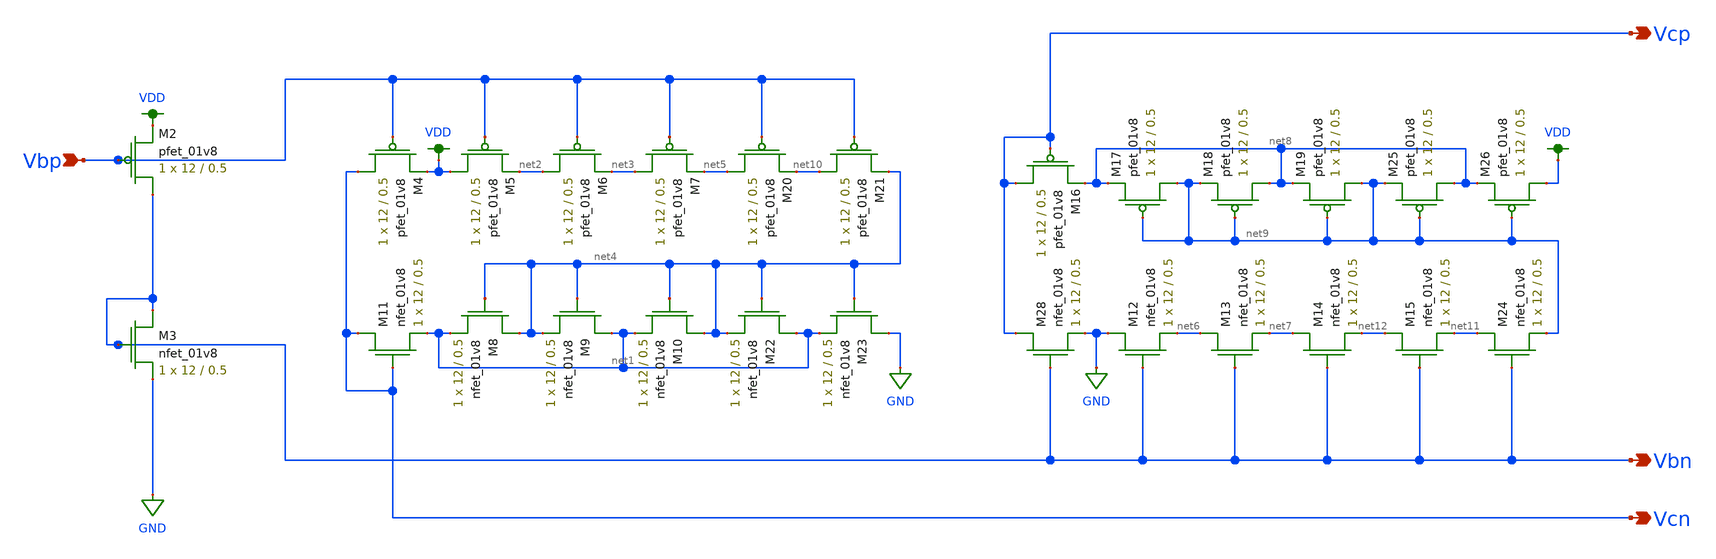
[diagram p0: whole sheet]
** sch_path: bias_current_generator.sch
**.subckt bias_current_generator Vcn Vbn Vcp Vbp
*.opin Vcn
*.opin Vbn
*.opin Vcp
*.ipin Vbp
XM4 Vcn Vbp VDD VDD sky130_fd_pr__pfet_01v8 L=0.5 W=12 nf=1 ad='int((nf+1)/2) * W/nf * 0.29' as='int((nf+2)/2) * W/nf * 0.29'
+ pd='2*int((nf+1)/2) * (W/nf + 0.29)' ps='2*int((nf+2)/2) * (W/nf + 0.29)' nrd='0.29 / W' nrs='0.29 / W'
+ sa=0 sb=0 sd=0 mult=1 m=1
XM11 Vcn Vcn net1 GND sky130_fd_pr__nfet_01v8 L=0.5 W=12 nf=1 ad='int((nf+1)/2) * W/nf * 0.29' as='int((nf+2)/2) * W/nf * 0.29'
+ pd='2*int((nf+1)/2) * (W/nf + 0.29)' ps='2*int((nf+2)/2) * (W/nf + 0.29)' nrd='0.29 / W' nrs='0.29 / W'
+ sa=0 sb=0 sd=0 mult=1 m=1
XM8 net4 net4 net1 GND sky130_fd_pr__nfet_01v8 L=0.5 W=12 nf=1 ad='int((nf+1)/2) * W/nf * 0.29' as='int((nf+2)/2) * W/nf * 0.29'
+ pd='2*int((nf+1)/2) * (W/nf + 0.29)' ps='2*int((nf+2)/2) * (W/nf + 0.29)' nrd='0.29 / W' nrs='0.29 / W'
+ sa=0 sb=0 sd=0 mult=1 m=1
XM9 net1 net4 net4 GND sky130_fd_pr__nfet_01v8 L=0.5 W=12 nf=1 ad='int((nf+1)/2) * W/nf * 0.29' as='int((nf+2)/2) * W/nf * 0.29'
+ pd='2*int((nf+1)/2) * (W/nf + 0.29)' ps='2*int((nf+2)/2) * (W/nf + 0.29)' nrd='0.29 / W' nrs='0.29 / W'
+ sa=0 sb=0 sd=0 mult=1 m=1
XM10 net4 net4 net1 GND sky130_fd_pr__nfet_01v8 L=0.5 W=12 nf=1 ad='int((nf+1)/2) * W/nf * 0.29' as='int((nf+2)/2) * W/nf * 0.29'
+ pd='2*int((nf+1)/2) * (W/nf + 0.29)' ps='2*int((nf+2)/2) * (W/nf + 0.29)' nrd='0.29 / W' nrs='0.29 / W'
+ sa=0 sb=0 sd=0 mult=1 m=1
XM22 net1 net4 net4 GND sky130_fd_pr__nfet_01v8 L=0.5 W=12 nf=1 ad='int((nf+1)/2) * W/nf * 0.29' as='int((nf+2)/2) * W/nf * 0.29'
+ pd='2*int((nf+1)/2) * (W/nf + 0.29)' ps='2*int((nf+2)/2) * (W/nf + 0.29)' nrd='0.29 / W' nrs='0.29 / W'
+ sa=0 sb=0 sd=0 mult=1 m=1
XM23 GND net4 net1 GND sky130_fd_pr__nfet_01v8 L=0.5 W=12 nf=1 ad='int((nf+1)/2) * W/nf * 0.29' as='int((nf+2)/2) * W/nf * 0.29'
+ pd='2*int((nf+1)/2) * (W/nf + 0.29)' ps='2*int((nf+2)/2) * (W/nf + 0.29)' nrd='0.29 / W' nrs='0.29 / W'
+ sa=0 sb=0 sd=0 mult=1 m=1
XM28 Vcp Vbn GND GND sky130_fd_pr__nfet_01v8 L=0.5 W=12 nf=1 ad='int((nf+1)/2) * W/nf * 0.29' as='int((nf+2)/2) * W/nf * 0.29'
+ pd='2*int((nf+1)/2) * (W/nf + 0.29)' ps='2*int((nf+2)/2) * (W/nf + 0.29)' nrd='0.29 / W' nrs='0.29 / W'
+ sa=0 sb=0 sd=0 mult=1 m=1
XM12 GND Vbn net6 GND sky130_fd_pr__nfet_01v8 L=0.5 W=12 nf=1 ad='int((nf+1)/2) * W/nf * 0.29' as='int((nf+2)/2) * W/nf * 0.29'
+ pd='2*int((nf+1)/2) * (W/nf + 0.29)' ps='2*int((nf+2)/2) * (W/nf + 0.29)' nrd='0.29 / W' nrs='0.29 / W'
+ sa=0 sb=0 sd=0 mult=1 m=1
XM13 net6 Vbn net7 GND sky130_fd_pr__nfet_01v8 L=0.5 W=12 nf=1 ad='int((nf+1)/2) * W/nf * 0.29' as='int((nf+2)/2) * W/nf * 0.29'
+ pd='2*int((nf+1)/2) * (W/nf + 0.29)' ps='2*int((nf+2)/2) * (W/nf + 0.29)' nrd='0.29 / W' nrs='0.29 / W'
+ sa=0 sb=0 sd=0 mult=1 m=1
XM14 net7 Vbn net12 GND sky130_fd_pr__nfet_01v8 L=0.5 W=12 nf=1 ad='int((nf+1)/2) * W/nf * 0.29' as='int((nf+2)/2) * W/nf * 0.29'
+ pd='2*int((nf+1)/2) * (W/nf + 0.29)' ps='2*int((nf+2)/2) * (W/nf + 0.29)' nrd='0.29 / W' nrs='0.29 / W'
+ sa=0 sb=0 sd=0 mult=1 m=1
XM15 net12 Vbn net11 GND sky130_fd_pr__nfet_01v8 L=0.5 W=12 nf=1 ad='int((nf+1)/2) * W/nf * 0.29' as='int((nf+2)/2) * W/nf * 0.29'
+ pd='2*int((nf+1)/2) * (W/nf + 0.29)' ps='2*int((nf+2)/2) * (W/nf + 0.29)' nrd='0.29 / W' nrs='0.29 / W'
+ sa=0 sb=0 sd=0 mult=1 m=1
XM24 net11 Vbn net9 GND sky130_fd_pr__nfet_01v8 L=0.5 W=12 nf=1 ad='int((nf+1)/2) * W/nf * 0.29' as='int((nf+2)/2) * W/nf * 0.29'
+ pd='2*int((nf+1)/2) * (W/nf + 0.29)' ps='2*int((nf+2)/2) * (W/nf + 0.29)' nrd='0.29 / W' nrs='0.29 / W'
+ sa=0 sb=0 sd=0 mult=1 m=1
XM5 VDD Vbp net2 VDD sky130_fd_pr__pfet_01v8 L=0.5 W=12 nf=1 ad='int((nf+1)/2) * W/nf * 0.29' as='int((nf+2)/2) * W/nf * 0.29'
+ pd='2*int((nf+1)/2) * (W/nf + 0.29)' ps='2*int((nf+2)/2) * (W/nf + 0.29)' nrd='0.29 / W' nrs='0.29 / W'
+ sa=0 sb=0 sd=0 mult=1 m=1
XM6 net2 Vbp net3 VDD sky130_fd_pr__pfet_01v8 L=0.5 W=12 nf=1 ad='int((nf+1)/2) * W/nf * 0.29' as='int((nf+2)/2) * W/nf * 0.29'
+ pd='2*int((nf+1)/2) * (W/nf + 0.29)' ps='2*int((nf+2)/2) * (W/nf + 0.29)' nrd='0.29 / W' nrs='0.29 / W'
+ sa=0 sb=0 sd=0 mult=1 m=1
XM7 net3 Vbp net5 VDD sky130_fd_pr__pfet_01v8 L=0.5 W=12 nf=1 ad='int((nf+1)/2) * W/nf * 0.29' as='int((nf+2)/2) * W/nf * 0.29'
+ pd='2*int((nf+1)/2) * (W/nf + 0.29)' ps='2*int((nf+2)/2) * (W/nf + 0.29)' nrd='0.29 / W' nrs='0.29 / W'
+ sa=0 sb=0 sd=0 mult=1 m=1
XM20 net5 Vbp net10 VDD sky130_fd_pr__pfet_01v8 L=0.5 W=12 nf=1 ad='int((nf+1)/2) * W/nf * 0.29' as='int((nf+2)/2) * W/nf * 0.29'
+ pd='2*int((nf+1)/2) * (W/nf + 0.29)' ps='2*int((nf+2)/2) * (W/nf + 0.29)' nrd='0.29 / W' nrs='0.29 / W'
+ sa=0 sb=0 sd=0 mult=1 m=1
XM21 net10 Vbp net4 VDD sky130_fd_pr__pfet_01v8 L=0.5 W=12 nf=1 ad='int((nf+1)/2) * W/nf * 0.29' as='int((nf+2)/2) * W/nf * 0.29'
+ pd='2*int((nf+1)/2) * (W/nf + 0.29)' ps='2*int((nf+2)/2) * (W/nf + 0.29)' nrd='0.29 / W' nrs='0.29 / W'
+ sa=0 sb=0 sd=0 mult=1 m=1
XM16 Vcp Vcp net8 VDD sky130_fd_pr__pfet_01v8 L=0.5 W=12 nf=1 ad='int((nf+1)/2) * W/nf * 0.29' as='int((nf+2)/2) * W/nf * 0.29'
+ pd='2*int((nf+1)/2) * (W/nf + 0.29)' ps='2*int((nf+2)/2) * (W/nf + 0.29)' nrd='0.29 / W' nrs='0.29 / W'
+ sa=0 sb=0 sd=0 mult=1 m=1
XM17 net9 net9 net8 VDD sky130_fd_pr__pfet_01v8 L=0.5 W=12 nf=1 ad='int((nf+1)/2) * W/nf * 0.29' as='int((nf+2)/2) * W/nf * 0.29'
+ pd='2*int((nf+1)/2) * (W/nf + 0.29)' ps='2*int((nf+2)/2) * (W/nf + 0.29)' nrd='0.29 / W' nrs='0.29 / W'
+ sa=0 sb=0 sd=0 mult=1 m=1
XM18 net8 net9 net9 VDD sky130_fd_pr__pfet_01v8 L=0.5 W=12 nf=1 ad='int((nf+1)/2) * W/nf * 0.29' as='int((nf+2)/2) * W/nf * 0.29'
+ pd='2*int((nf+1)/2) * (W/nf + 0.29)' ps='2*int((nf+2)/2) * (W/nf + 0.29)' nrd='0.29 / W' nrs='0.29 / W'
+ sa=0 sb=0 sd=0 mult=1 m=1
XM19 net9 net9 net8 VDD sky130_fd_pr__pfet_01v8 L=0.5 W=12 nf=1 ad='int((nf+1)/2) * W/nf * 0.29' as='int((nf+2)/2) * W/nf * 0.29'
+ pd='2*int((nf+1)/2) * (W/nf + 0.29)' ps='2*int((nf+2)/2) * (W/nf + 0.29)' nrd='0.29 / W' nrs='0.29 / W'
+ sa=0 sb=0 sd=0 mult=1 m=1
XM25 net8 net9 net9 VDD sky130_fd_pr__pfet_01v8 L=0.5 W=12 nf=1 ad='int((nf+1)/2) * W/nf * 0.29' as='int((nf+2)/2) * W/nf * 0.29'
+ pd='2*int((nf+1)/2) * (W/nf + 0.29)' ps='2*int((nf+2)/2) * (W/nf + 0.29)' nrd='0.29 / W' nrs='0.29 / W'
+ sa=0 sb=0 sd=0 mult=1 m=1
XM26 VDD net9 net8 VDD sky130_fd_pr__pfet_01v8 L=0.5 W=12 nf=1 ad='int((nf+1)/2) * W/nf * 0.29' as='int((nf+2)/2) * W/nf * 0.29'
+ pd='2*int((nf+1)/2) * (W/nf + 0.29)' ps='2*int((nf+2)/2) * (W/nf + 0.29)' nrd='0.29 / W' nrs='0.29 / W'
+ sa=0 sb=0 sd=0 mult=1 m=1
XM2 Vbn Vbp VDD VDD sky130_fd_pr__pfet_01v8 L=0.5 W=12 nf=1 ad='int((nf+1)/2) * W/nf * 0.29' as='int((nf+2)/2) * W/nf * 0.29'
+ pd='2*int((nf+1)/2) * (W/nf + 0.29)' ps='2*int((nf+2)/2) * (W/nf + 0.29)' nrd='0.29 / W' nrs='0.29 / W'
+ sa=0 sb=0 sd=0 mult=1 m=1
XM3 Vbn Vbn GND GND sky130_fd_pr__nfet_01v8 L=0.5 W=12 nf=1 ad='int((nf+1)/2) * W/nf * 0.29' as='int((nf+2)/2) * W/nf * 0.29'
+ pd='2*int((nf+1)/2) * (W/nf + 0.29)' ps='2*int((nf+2)/2) * (W/nf + 0.29)' nrd='0.29 / W' nrs='0.29 / W'
+ sa=0 sb=0 sd=0 mult=1 m=1
**.ends
.GLOBAL GND
.GLOBAL VDD
.end
